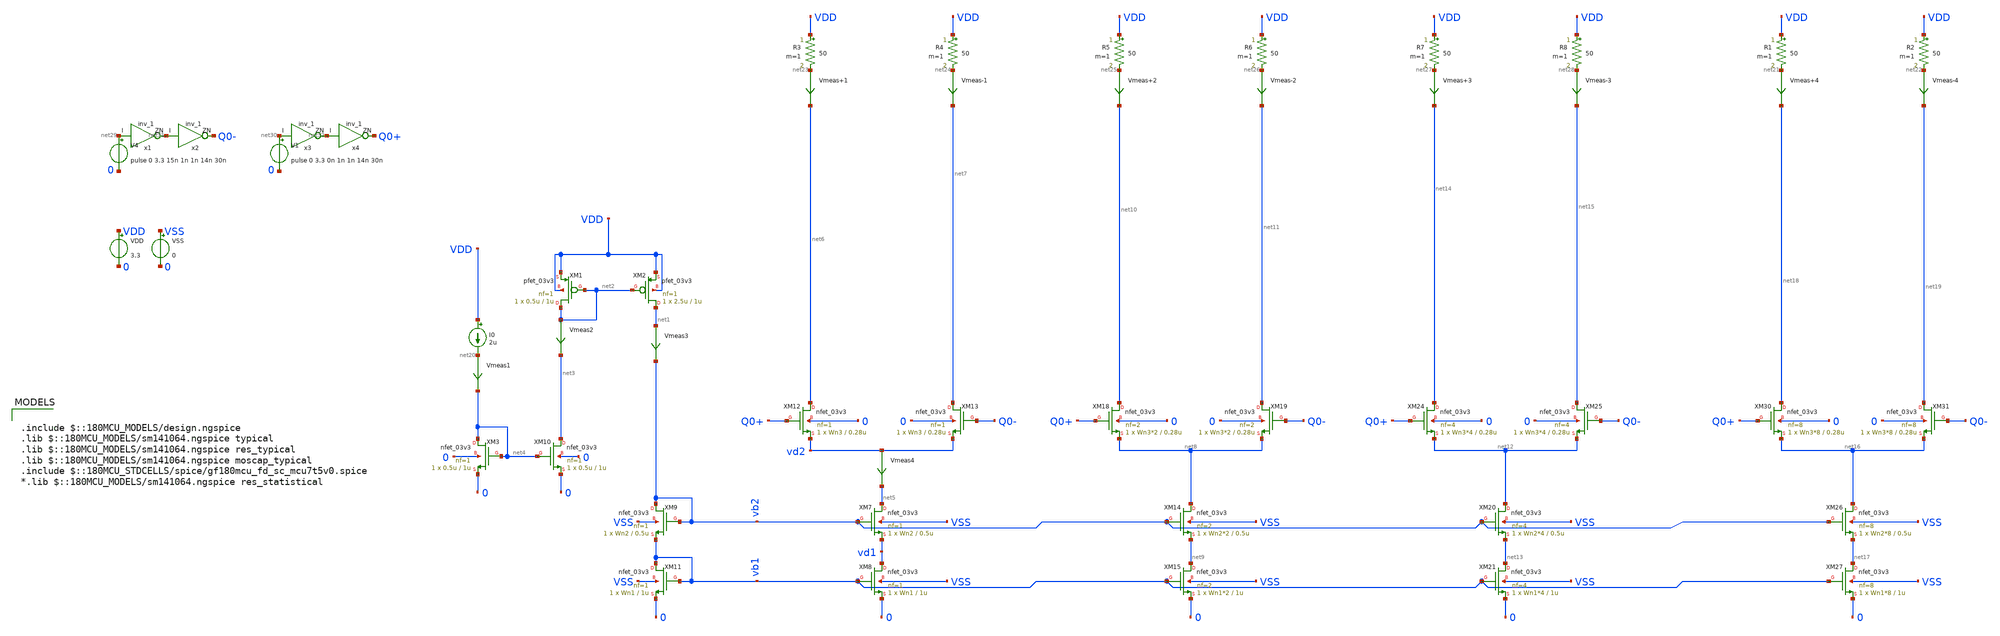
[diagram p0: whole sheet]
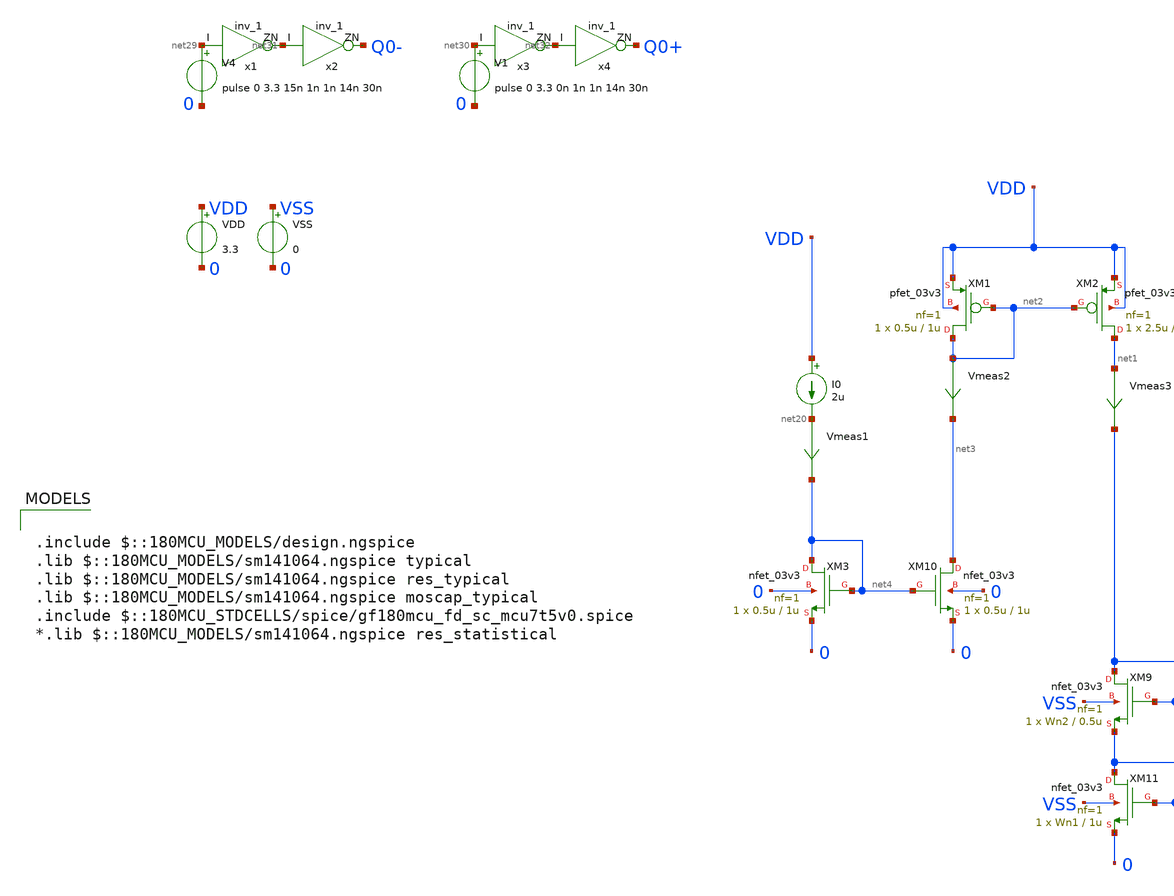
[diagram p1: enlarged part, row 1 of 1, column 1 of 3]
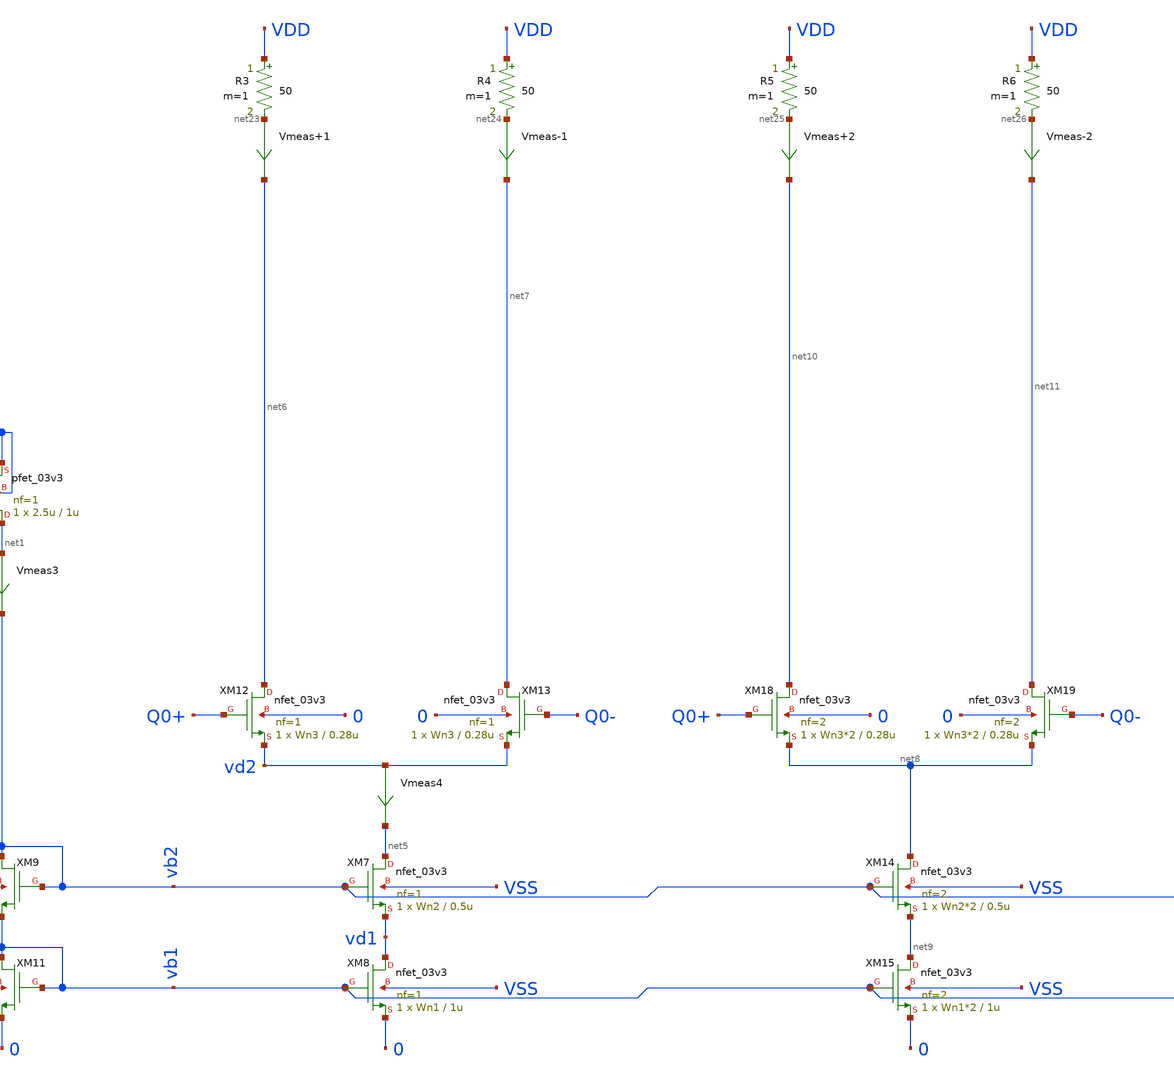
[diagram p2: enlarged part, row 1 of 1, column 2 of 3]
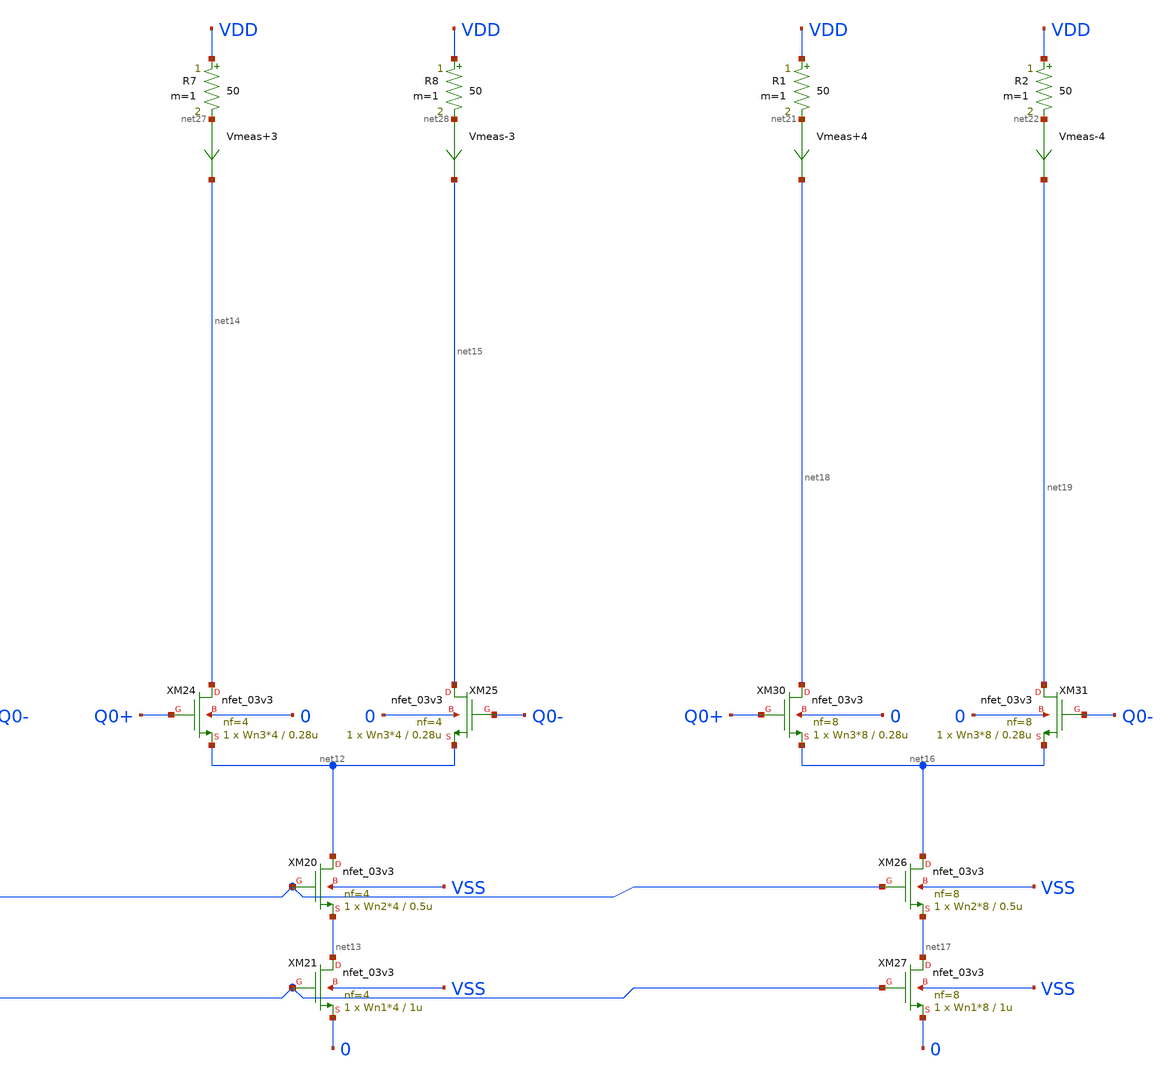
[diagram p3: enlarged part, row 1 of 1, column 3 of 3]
** sch_path: xschem/test_finger.sch
**.subckt test_finger
XM1 net2 net2 VDD VDD pfet_03v3 L=1u W=0.5u nf=1 ad='int((nf+1)/2) * W/nf * 0.18u' as='int((nf+2)/2) * W/nf * 0.18u'
+ pd='2*int((nf+1)/2) * (W/nf + 0.18u)' ps='2*int((nf+2)/2) * (W/nf + 0.18u)' nrd='0.18u / W' nrs='0.18u / W'
+ sa=0 sb=0 sd=0 m=1
XM2 net1 net2 VDD VDD pfet_03v3 L=1u W=2.5u nf=1 ad='int((nf+1)/2) * W/nf * 0.18u' as='int((nf+2)/2) * W/nf * 0.18u'
+ pd='2*int((nf+1)/2) * (W/nf + 0.18u)' ps='2*int((nf+2)/2) * (W/nf + 0.18u)' nrd='0.18u / W' nrs='0.18u / W'
+ sa=0 sb=0 sd=0 m=1
I0 VDD net20 2u
XM3 net4 net4 0 0 nfet_03v3 L=1u W=0.5u nf=1 ad='int((nf+1)/2) * W/nf * 0.18u' as='int((nf+2)/2) * W/nf * 0.18u'
+ pd='2*int((nf+1)/2) * (W/nf + 0.18u)' ps='2*int((nf+2)/2) * (W/nf + 0.18u)' nrd='0.18u / W' nrs='0.18u / W'
+ sa=0 sb=0 sd=0 m=1
XM10 net3 net4 0 0 nfet_03v3 L=1u W=0.5u nf=1 ad='int((nf+1)/2) * W/nf * 0.18u' as='int((nf+2)/2) * W/nf * 0.18u'
+ pd='2*int((nf+1)/2) * (W/nf + 0.18u)' ps='2*int((nf+2)/2) * (W/nf + 0.18u)' nrd='0.18u / W' nrs='0.18u / W'
+ sa=0 sb=0 sd=0 m=1
Vmeas1 net20 net4 0
.save i(vmeas1)
XM7 net5 vb2 vd1 VSS nfet_03v3 L=0.5u W=Wn2 nf=1 ad='int((nf+1)/2) * W/nf * 0.18u' as='int((nf+2)/2) * W/nf * 0.18u'
+ pd='2*int((nf+1)/2) * (W/nf + 0.18u)' ps='2*int((nf+2)/2) * (W/nf + 0.18u)' nrd='0.18u / W' nrs='0.18u / W'
+ sa=0 sb=0 sd=0 m=1
XM8 vd1 vb1 0 VSS nfet_03v3 L=1u W=Wn1 nf=1 ad='int((nf+1)/2) * W/nf * 0.18u' as='int((nf+2)/2) * W/nf * 0.18u'
+ pd='2*int((nf+1)/2) * (W/nf + 0.18u)' ps='2*int((nf+2)/2) * (W/nf + 0.18u)' nrd='0.18u / W' nrs='0.18u / W'
+ sa=0 sb=0 sd=0 m=1
XM9 vb2 vb2 vb1 VSS nfet_03v3 L=0.5u W=Wn2 nf=1 ad='int((nf+1)/2) * W/nf * 0.18u' as='int((nf+2)/2) * W/nf * 0.18u'
+ pd='2*int((nf+1)/2) * (W/nf + 0.18u)' ps='2*int((nf+2)/2) * (W/nf + 0.18u)' nrd='0.18u / W' nrs='0.18u / W'
+ sa=0 sb=0 sd=0 m=1
XM11 vb1 vb1 0 VSS nfet_03v3 L=1u W=Wn1 nf=1 ad='int((nf+1)/2) * W/nf * 0.18u' as='int((nf+2)/2) * W/nf * 0.18u'
+ pd='2*int((nf+1)/2) * (W/nf + 0.18u)' ps='2*int((nf+2)/2) * (W/nf + 0.18u)' nrd='0.18u / W' nrs='0.18u / W'
+ sa=0 sb=0 sd=0 m=1
XM12 net6 Q0+ vd2 0 nfet_03v3 L=0.28u W=Wn3 nf=1 ad='int((nf+1)/2) * W/nf * 0.18u' as='int((nf+2)/2) * W/nf * 0.18u'
+ pd='2*int((nf+1)/2) * (W/nf + 0.18u)' ps='2*int((nf+2)/2) * (W/nf + 0.18u)' nrd='0.18u / W' nrs='0.18u / W'
+ sa=0 sb=0 sd=0 m=1
XM13 net7 Q0- vd2 0 nfet_03v3 L=0.28u W=Wn3 nf=1 ad='int((nf+1)/2) * W/nf * 0.18u' as='int((nf+2)/2) * W/nf * 0.18u'
+ pd='2*int((nf+1)/2) * (W/nf + 0.18u)' ps='2*int((nf+2)/2) * (W/nf + 0.18u)' nrd='0.18u / W' nrs='0.18u / W'
+ sa=0 sb=0 sd=0 m=1
Vmeas2 net2 net3 0
.save i(vmeas2)
Vmeas3 net1 vb2 0
.save i(vmeas3)
Vmeas4 vd2 net5 0
.save i(vmeas4)
R1 VDD net21 50 m=1
R2 VDD net22 50 m=1
Vmeas+4 net21 net18 0
.save i(vmeas+4)
Vmeas-4 net22 net19 0
.save i(vmeas-4)
XM14 net8 vb2 net9 VSS nfet_03v3 L=0.5u W=Wn2*2 nf=2 ad='int((nf+1)/2) * W/nf * 0.18u' as='int((nf+2)/2) * W/nf * 0.18u'
+ pd='2*int((nf+1)/2) * (W/nf + 0.18u)' ps='2*int((nf+2)/2) * (W/nf + 0.18u)' nrd='0.18u / W' nrs='0.18u / W'
+ sa=0 sb=0 sd=0 m=1
XM15 net9 vb1 0 VSS nfet_03v3 L=1u W=Wn1*2 nf=2 ad='int((nf+1)/2) * W/nf * 0.18u' as='int((nf+2)/2) * W/nf * 0.18u'
+ pd='2*int((nf+1)/2) * (W/nf + 0.18u)' ps='2*int((nf+2)/2) * (W/nf + 0.18u)' nrd='0.18u / W' nrs='0.18u / W'
+ sa=0 sb=0 sd=0 m=1
XM18 net10 Q0+ net8 0 nfet_03v3 L=0.28u W=Wn3*2 nf=2 ad='int((nf+1)/2) * W/nf * 0.18u' as='int((nf+2)/2) * W/nf * 0.18u'
+ pd='2*int((nf+1)/2) * (W/nf + 0.18u)' ps='2*int((nf+2)/2) * (W/nf + 0.18u)' nrd='0.18u / W' nrs='0.18u / W'
+ sa=0 sb=0 sd=0 m=1
XM19 net11 Q0- net8 0 nfet_03v3 L=0.28u W=Wn3*2 nf=2 ad='int((nf+1)/2) * W/nf * 0.18u' as='int((nf+2)/2) * W/nf * 0.18u'
+ pd='2*int((nf+1)/2) * (W/nf + 0.18u)' ps='2*int((nf+2)/2) * (W/nf + 0.18u)' nrd='0.18u / W' nrs='0.18u / W'
+ sa=0 sb=0 sd=0 m=1
R3 VDD net23 50 m=1
R4 VDD net24 50 m=1
Vmeas+1 net23 net6 0
.save i(vmeas+1)
Vmeas-1 net24 net7 0
.save i(vmeas-1)
XM20 net12 vb2 net13 VSS nfet_03v3 L=0.5u W=Wn2*4 nf=4 ad='int((nf+1)/2) * W/nf * 0.18u' as='int((nf+2)/2) * W/nf * 0.18u'
+ pd='2*int((nf+1)/2) * (W/nf + 0.18u)' ps='2*int((nf+2)/2) * (W/nf + 0.18u)' nrd='0.18u / W' nrs='0.18u / W'
+ sa=0 sb=0 sd=0 m=1
XM21 net13 vb1 0 VSS nfet_03v3 L=1u W=Wn1*4 nf=4 ad='int((nf+1)/2) * W/nf * 0.18u' as='int((nf+2)/2) * W/nf * 0.18u'
+ pd='2*int((nf+1)/2) * (W/nf + 0.18u)' ps='2*int((nf+2)/2) * (W/nf + 0.18u)' nrd='0.18u / W' nrs='0.18u / W'
+ sa=0 sb=0 sd=0 m=1
XM24 net14 Q0+ net12 0 nfet_03v3 L=0.28u W=Wn3*4 nf=4 ad='int((nf+1)/2) * W/nf * 0.18u' as='int((nf+2)/2) * W/nf * 0.18u'
+ pd='2*int((nf+1)/2) * (W/nf + 0.18u)' ps='2*int((nf+2)/2) * (W/nf + 0.18u)' nrd='0.18u / W' nrs='0.18u / W'
+ sa=0 sb=0 sd=0 m=1
XM25 net15 Q0- net12 0 nfet_03v3 L=0.28u W=Wn3*4 nf=4 ad='int((nf+1)/2) * W/nf * 0.18u' as='int((nf+2)/2) * W/nf * 0.18u'
+ pd='2*int((nf+1)/2) * (W/nf + 0.18u)' ps='2*int((nf+2)/2) * (W/nf + 0.18u)' nrd='0.18u / W' nrs='0.18u / W'
+ sa=0 sb=0 sd=0 m=1
XM26 net16 vb2 net17 VSS nfet_03v3 L=0.5u W=Wn2*8 nf=8 ad='int((nf+1)/2) * W/nf * 0.18u' as='int((nf+2)/2) * W/nf * 0.18u'
+ pd='2*int((nf+1)/2) * (W/nf + 0.18u)' ps='2*int((nf+2)/2) * (W/nf + 0.18u)' nrd='0.18u / W' nrs='0.18u / W'
+ sa=0 sb=0 sd=0 m=1
XM27 net17 vb1 0 VSS nfet_03v3 L=1u W=Wn1*8 nf=8 ad='int((nf+1)/2) * W/nf * 0.18u' as='int((nf+2)/2) * W/nf * 0.18u'
+ pd='2*int((nf+1)/2) * (W/nf + 0.18u)' ps='2*int((nf+2)/2) * (W/nf + 0.18u)' nrd='0.18u / W' nrs='0.18u / W'
+ sa=0 sb=0 sd=0 m=1
XM30 net18 Q0+ net16 0 nfet_03v3 L=0.28u W=Wn3*8 nf=8 ad='int((nf+1)/2) * W/nf * 0.18u' as='int((nf+2)/2) * W/nf * 0.18u'
+ pd='2*int((nf+1)/2) * (W/nf + 0.18u)' ps='2*int((nf+2)/2) * (W/nf + 0.18u)' nrd='0.18u / W' nrs='0.18u / W'
+ sa=0 sb=0 sd=0 m=1
XM31 net19 Q0- net16 0 nfet_03v3 L=0.28u W=Wn3*8 nf=8 ad='int((nf+1)/2) * W/nf * 0.18u' as='int((nf+2)/2) * W/nf * 0.18u'
+ pd='2*int((nf+1)/2) * (W/nf + 0.18u)' ps='2*int((nf+2)/2) * (W/nf + 0.18u)' nrd='0.18u / W' nrs='0.18u / W'
+ sa=0 sb=0 sd=0 m=1
R5 VDD net25 50 m=1
R6 VDD net26 50 m=1
Vmeas+2 net25 net10 0
.save i(vmeas+2)
Vmeas-2 net26 net11 0
.save i(vmeas-2)
R7 VDD net27 50 m=1
R8 VDD net28 50 m=1
Vmeas+3 net27 net14 0
.save i(vmeas+3)
Vmeas-3 net28 net15 0
.save i(vmeas-3)
VDD VDD 0 3.3
VSS VSS 0 0
V4 net29 0 pulse 0 3.3 15n 1n 1n 14n 30n
V1 net30 0 pulse 0 3.3 0n 1n 1n 14n 30n
x1 net29 net31 VDD VNW VPW VSS gf180mcu_fd_sc_mcu7t5v0__inv_1
x2 net31 Q0- VDD VNW VPW VSS gf180mcu_fd_sc_mcu7t5v0__inv_1
x3 net30 net32 VDD VNW VPW VSS gf180mcu_fd_sc_mcu7t5v0__inv_1
x4 net32 Q0+ VDD VNW VPW VSS gf180mcu_fd_sc_mcu7t5v0__inv_1
**** begin user architecture code


.param Mn1=1
.param Mn2=1
.param Mn3=1
.param Mn4=1
.param nf1=1
.param nf2=2
.param nf3=3
.param nf4=4

.param Wn1=2u
.param Wn2=2u
.param Wn3=1u
.save @m.xm7.m0[vth] @m.xm8.m0[vth] @m.xm27.m0[vth] @m.xm26.m0[vth] @m.xm30.m0[vth]
.options savecurrents

.control
	tran 0.5n 100n
	*plot i(Vmeas1) i(Vmeas2) i(Vmeas3) i(Vmeas4)
	*plot v(vb2) v(vb1) v(vd1) v(vd2)
	plot i(Vmeas+1) i(Vmeas-1) i(Vmeas+2) i(Vmeas-2) i(Vmeas+3) i(Vmeas-3) i(Vmeas+4) i(Vmeas-4)
	*plot v(vb1)-@m.xm8.m0[vth]
	*plot v(vb2)-v(vd1)-@m.xm7.m0[vth]
	plot v(vb1)-@m.xm8.m0[vth] v(vb2)-v(vd1)-@m.xm7.m0[vth] v(q0+)-v(vd2)-@m.xm12.m0[vth]
	*plot v(q0+)-v(vd2)-@m.xm12.m0[vth]
	*plot @m.xm26.m0[vth] @m.xm27.m0[vth] @m.xm30.m0[vth]
	write test_finger.raw
.endc

.save all



.include $::180MCU_MODELS/design.ngspice
.lib $::180MCU_MODELS/sm141064.ngspice typical
.lib $::180MCU_MODELS/sm141064.ngspice res_typical
.lib $::180MCU_MODELS/sm141064.ngspice moscap_typical
.include $::180MCU_STDCELLS/spice/gf180mcu_fd_sc_mcu7t5v0.spice
*.lib $::180MCU_MODELS/sm141064.ngspice res_statistical

**** end user architecture code
**.ends
.end
